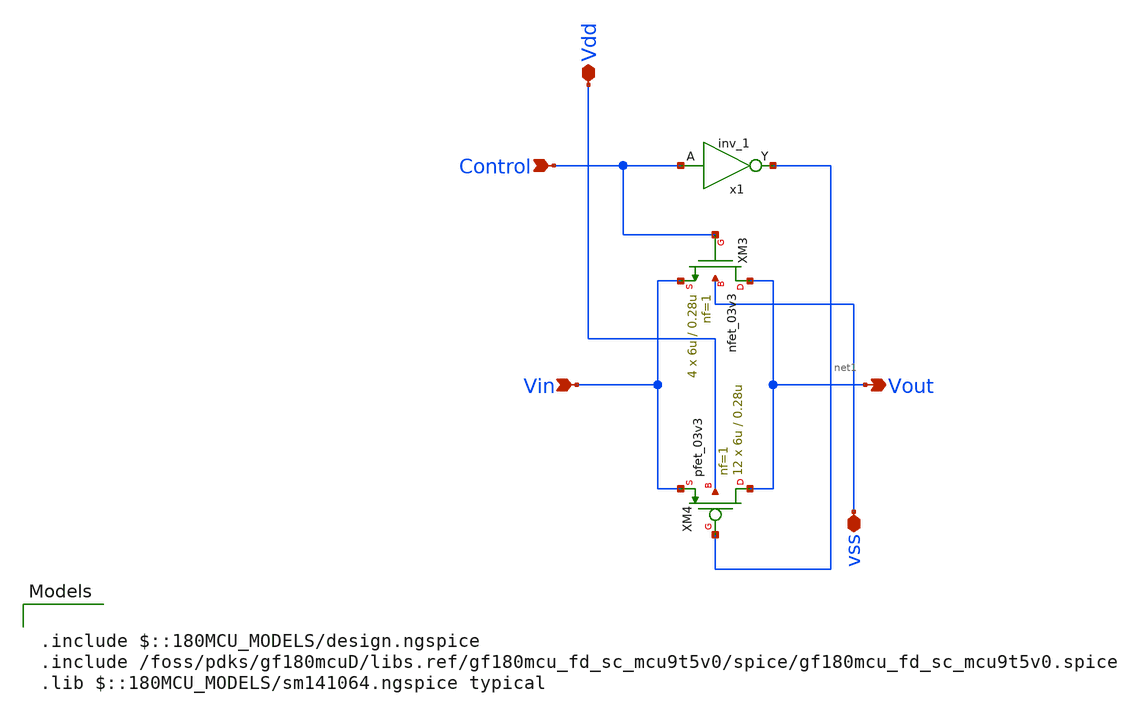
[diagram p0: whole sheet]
** sch_path: designs/libs/core_analog/tx_gate/transmission_gate_2.sch
**.subckt transmission_gate_2 Vdd Control Vout Vin vss
*.iopin Vdd
*.ipin Control
*.opin Vout
*.ipin Vin
*.iopin vss
XM3 Vout Control Vin vss nfet_03v3 L=0.28u W=6u nf=1 ad='int((nf+1)/2) * W/nf * 0.18u' as='int((nf+2)/2) * W/nf * 0.18u'
+ pd='2*int((nf+1)/2) * (W/nf + 0.18u)' ps='2*int((nf+2)/2) * (W/nf + 0.18u)' nrd='0.18u / W' nrs='0.18u / W'
+ sa=0 sb=0 sd=0 m=4
XM4 Vout net1 Vin Vdd pfet_03v3 L=0.28u W=6u nf=1 ad='int((nf+1)/2) * W/nf * 0.18u' as='int((nf+2)/2) * W/nf * 0.18u'
+ pd='2*int((nf+1)/2) * (W/nf + 0.18u)' ps='2*int((nf+2)/2) * (W/nf + 0.18u)' nrd='0.18u / W' nrs='0.18u / W'
+ sa=0 sb=0 sd=0 m=12
x1 Control VSSd VDDd VSSd VDDd net1 gf180mcu_fd_sc_mcu9t5v0__inv_1
**** begin user architecture code

.include $::180MCU_MODELS/design.ngspice
.include /foss/pdks/gf180mcuD/libs.ref/gf180mcu_fd_sc_mcu9t5v0/spice/gf180mcu_fd_sc_mcu9t5v0.spice
.lib $::180MCU_MODELS/sm141064.ngspice typical

**** end user architecture code
**.ends
.end
